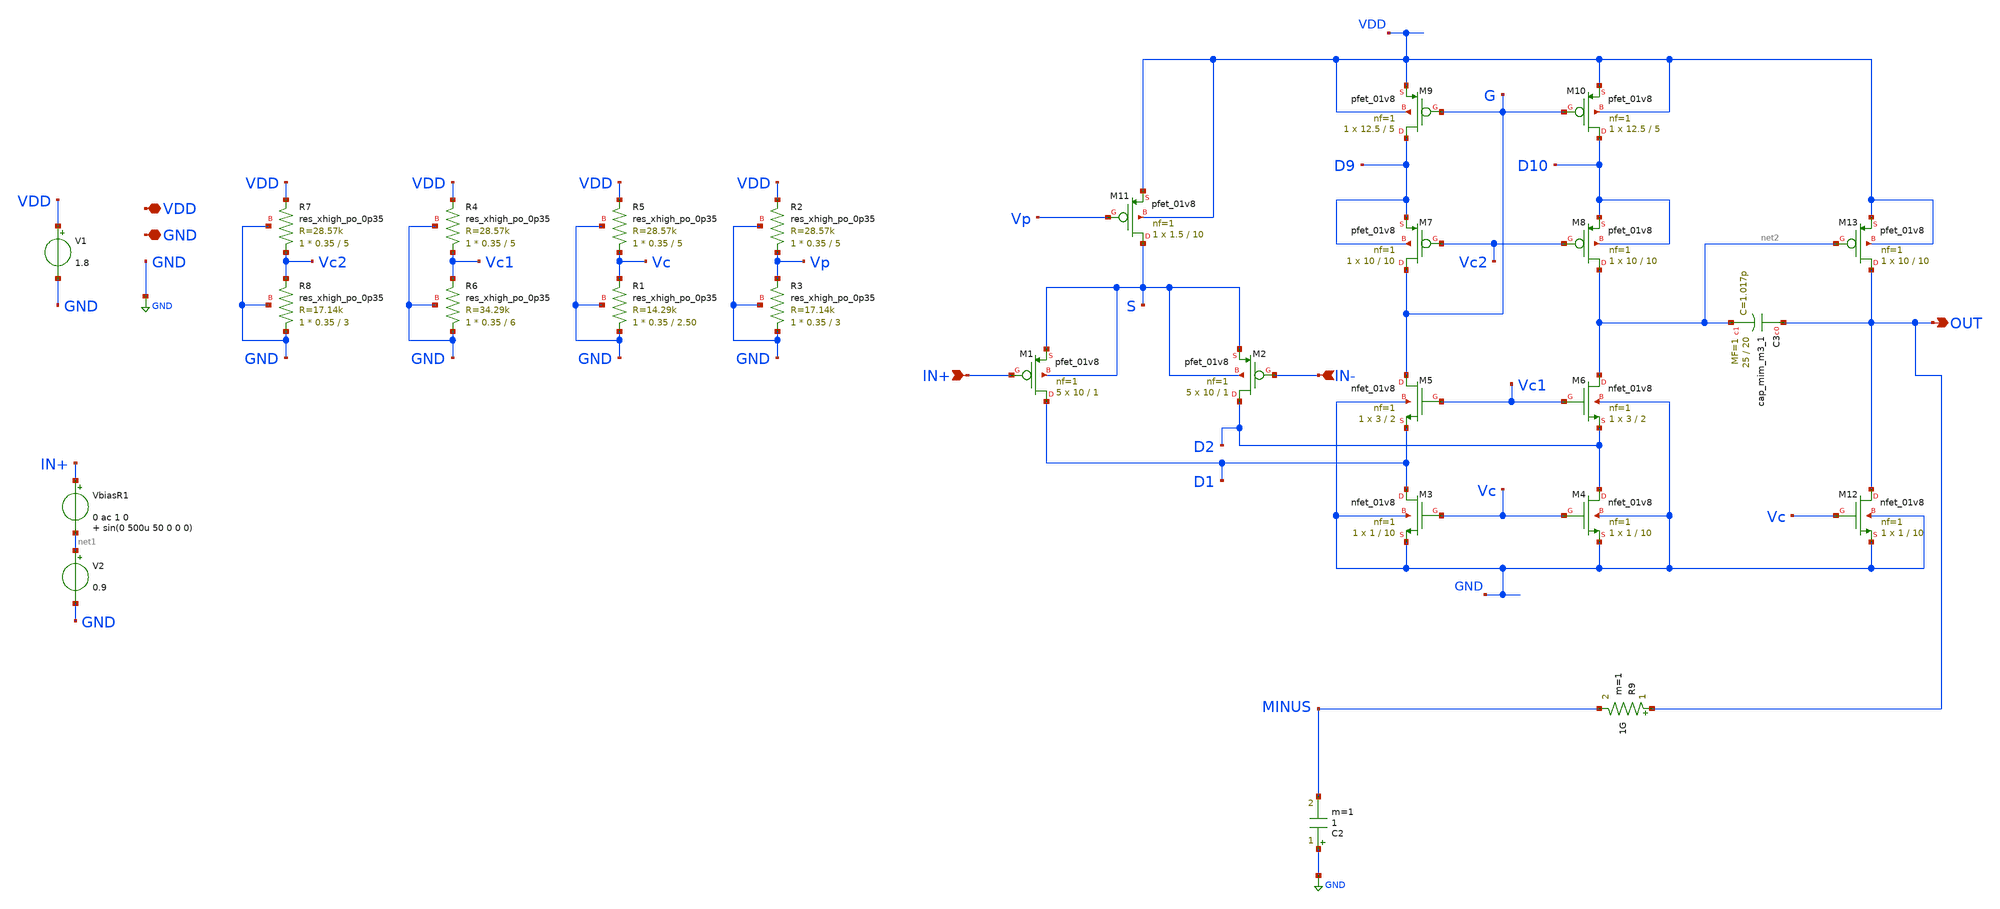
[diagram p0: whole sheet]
** sch_path: xschem/OpAmp_FoldedCascode_Noise0.sch
**.subckt OpAmp_FoldedCascode_Noise0 VDD GND IN+ IN- OUT
*.iopin VDD
*.iopin GND
*.ipin IN+
*.ipin IN-
*.opin OUT
VbiasR1 IN+ net1 0 ac 1 0 sin(0 500u 50 0 0 0)
V2 net1 GND 0.9
V1 VDD GND 1.8
XR5 Vc VDD GND sky130_fd_pr__res_xhigh_po_0p35 L=5 mult=1 m=1
XR1 GND Vc GND sky130_fd_pr__res_xhigh_po_0p35 L=2.50 mult=1 m=1
XR2 Vp VDD GND sky130_fd_pr__res_xhigh_po_0p35 L=5 mult=1 m=1
XR3 GND Vp GND sky130_fd_pr__res_xhigh_po_0p35 L=3 mult=1 m=1
XR4 Vc1 VDD GND sky130_fd_pr__res_xhigh_po_0p35 L=5 mult=1 m=1
XR6 GND Vc1 GND sky130_fd_pr__res_xhigh_po_0p35 L=6 mult=1 m=1
XR7 Vc2 VDD GND sky130_fd_pr__res_xhigh_po_0p35 L=5 mult=1 m=1
XR8 GND Vc2 GND sky130_fd_pr__res_xhigh_po_0p35 L=3 mult=1 m=1
C2 GND MINUS 1 m=1
R9 OUT MINUS 1G m=1
XM1 D1 IN+ S S sky130_fd_pr__pfet_01v8 L=1 W=10 nf=1 ad='int((nf+1)/2) * W/nf * 0.29' as='int((nf+2)/2) * W/nf * 0.29'
+ pd='2*int((nf+1)/2) * (W/nf + 0.29)' ps='2*int((nf+2)/2) * (W/nf + 0.29)' nrd='0.29 / W' nrs='0.29 / W'
+ sa=0 sb=0 sd=0 mult=5 m=5
XM2 D2 IN- S S sky130_fd_pr__pfet_01v8 L=1 W=10 nf=1 ad='int((nf+1)/2) * W/nf * 0.29' as='int((nf+2)/2) * W/nf * 0.29'
+ pd='2*int((nf+1)/2) * (W/nf + 0.29)' ps='2*int((nf+2)/2) * (W/nf + 0.29)' nrd='0.29 / W' nrs='0.29 / W'
+ sa=0 sb=0 sd=0 mult=5 m=5
XM3 D1 Vc GND GND sky130_fd_pr__nfet_01v8 L=10 W=1 nf=1 ad='int((nf+1)/2) * W/nf * 0.29' as='int((nf+2)/2) * W/nf * 0.29'
+ pd='2*int((nf+1)/2) * (W/nf + 0.29)' ps='2*int((nf+2)/2) * (W/nf + 0.29)' nrd='0.29 / W' nrs='0.29 / W'
+ sa=0 sb=0 sd=0 mult=1 m=1
XM4 D2 Vc GND GND sky130_fd_pr__nfet_01v8 L=10 W=1 nf=1 ad='int((nf+1)/2) * W/nf * 0.29' as='int((nf+2)/2) * W/nf * 0.29'
+ pd='2*int((nf+1)/2) * (W/nf + 0.29)' ps='2*int((nf+2)/2) * (W/nf + 0.29)' nrd='0.29 / W' nrs='0.29 / W'
+ sa=0 sb=0 sd=0 mult=1 m=1
XM5 G Vc1 D1 GND sky130_fd_pr__nfet_01v8 L=2 W=3 nf=1 ad='int((nf+1)/2) * W/nf * 0.29' as='int((nf+2)/2) * W/nf * 0.29'
+ pd='2*int((nf+1)/2) * (W/nf + 0.29)' ps='2*int((nf+2)/2) * (W/nf + 0.29)' nrd='0.29 / W' nrs='0.29 / W'
+ sa=0 sb=0 sd=0 mult=1 m=1
XM6 net2 Vc1 D2 GND sky130_fd_pr__nfet_01v8 L=2 W=3 nf=1 ad='int((nf+1)/2) * W/nf * 0.29' as='int((nf+2)/2) * W/nf * 0.29'
+ pd='2*int((nf+1)/2) * (W/nf + 0.29)' ps='2*int((nf+2)/2) * (W/nf + 0.29)' nrd='0.29 / W' nrs='0.29 / W'
+ sa=0 sb=0 sd=0 mult=1 m=1
XM7 G Vc2 D9 D9 sky130_fd_pr__pfet_01v8 L=10 W=10 nf=1 ad='int((nf+1)/2) * W/nf * 0.29' as='int((nf+2)/2) * W/nf * 0.29'
+ pd='2*int((nf+1)/2) * (W/nf + 0.29)' ps='2*int((nf+2)/2) * (W/nf + 0.29)' nrd='0.29 / W' nrs='0.29 / W'
+ sa=0 sb=0 sd=0 mult=1 m=1
XM8 net2 Vc2 D10 D10 sky130_fd_pr__pfet_01v8 L=10 W=10 nf=1 ad='int((nf+1)/2) * W/nf * 0.29' as='int((nf+2)/2) * W/nf * 0.29'
+ pd='2*int((nf+1)/2) * (W/nf + 0.29)' ps='2*int((nf+2)/2) * (W/nf + 0.29)' nrd='0.29 / W' nrs='0.29 / W'
+ sa=0 sb=0 sd=0 mult=1 m=1
XM9 D9 G VDD VDD sky130_fd_pr__pfet_01v8 L=5 W=12.5 nf=1 ad='int((nf+1)/2) * W/nf * 0.29' as='int((nf+2)/2) * W/nf * 0.29'
+ pd='2*int((nf+1)/2) * (W/nf + 0.29)' ps='2*int((nf+2)/2) * (W/nf + 0.29)' nrd='0.29 / W' nrs='0.29 / W'
+ sa=0 sb=0 sd=0 mult=1 m=1
XM10 D10 G VDD VDD sky130_fd_pr__pfet_01v8 L=5 W=12.5 nf=1 ad='int((nf+1)/2) * W/nf * 0.29' as='int((nf+2)/2) * W/nf * 0.29'
+ pd='2*int((nf+1)/2) * (W/nf + 0.29)' ps='2*int((nf+2)/2) * (W/nf + 0.29)' nrd='0.29 / W' nrs='0.29 / W'
+ sa=0 sb=0 sd=0 mult=1 m=1
XM11 S Vp VDD VDD sky130_fd_pr__pfet_01v8 L=10 W=1.5 nf=1 ad='int((nf+1)/2) * W / nf * 0.29' as='int((nf+2)/2) * W / nf * 0.29'
+ pd='2*int((nf+1)/2) * (W / nf + 0.29)' ps='2*int((nf+2)/2) * (W / nf + 0.29)' nrd='0.29 / W ' nrs='0.29 / W '
+ sa=0 sb=0 sd=0 mult=1 m=1
XM12 OUT Vc GND GND sky130_fd_pr__nfet_01v8 L=10 W=1 nf=1 ad='int((nf+1)/2) * W/nf * 0.29' as='int((nf+2)/2) * W/nf * 0.29'
+ pd='2*int((nf+1)/2) * (W/nf + 0.29)' ps='2*int((nf+2)/2) * (W/nf + 0.29)' nrd='0.29 / W' nrs='0.29 / W'
+ sa=0 sb=0 sd=0 mult=1 m=1
XM13 OUT net2 VDD VDD sky130_fd_pr__pfet_01v8 L=10 W=10 nf=1 ad='int((nf+1)/2) * W/nf * 0.29' as='int((nf+2)/2) * W/nf * 0.29'
+ pd='2*int((nf+1)/2) * (W/nf + 0.29)' ps='2*int((nf+2)/2) * (W/nf + 0.29)' nrd='0.29 / W' nrs='0.29 / W'
+ sa=0 sb=0 sd=0 mult=1 m=1
XC3 OUT net2 sky130_fd_pr__cap_mim_m3_1 W=25 L=20 MF=1 m=1
**** begin user architecture code



.option reltol=1e-5   abstol=1e-14 savecurrents
.control
  save all
  op
  remzerovec
  write OpAmp_FoldedCascode_Noise0.raw

  set appendwrite
  noise v(OUT) VbiasR1 dec 10 0.01 1e3
  remzerovec
  write OpAmp_FoldedCascode_Noise0.raw

.endc



.lib $::SKYWATER_MODELS/sky130.lib.spice tt
**** end user architecture code
**.ends
.GLOBAL GND
.end
